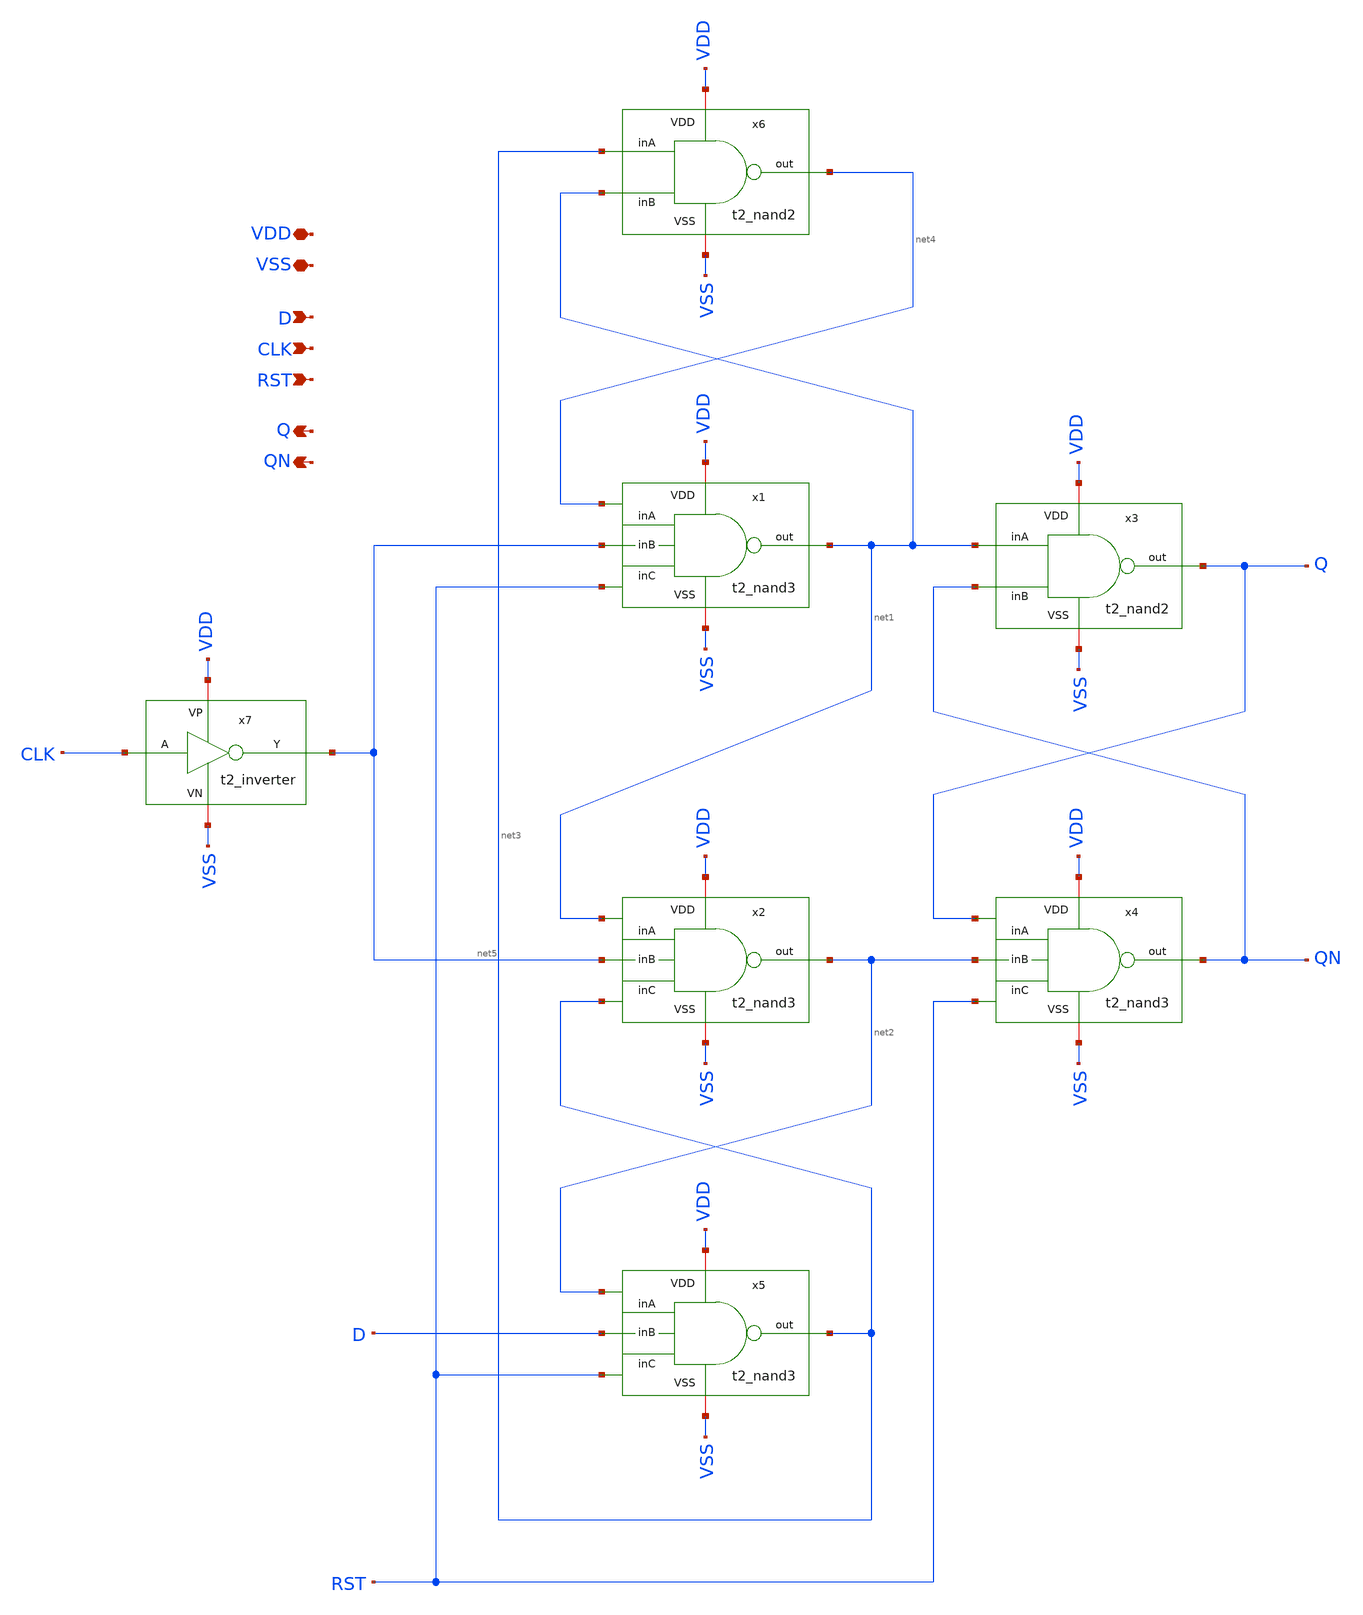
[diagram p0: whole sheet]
** sch_path: Team 2 Design/design_data/xschem/t2_dff_1.sch
**.subckt t2_dff_1 VSS D RST Q VDD QN CLK
*.iopin VSS
*.ipin D
*.ipin RST
*.opin Q
*.iopin VDD
*.opin QN
*.ipin CLK
x3 VDD net1 QN Q VSS t2_nand2
x4 VDD VSS Q net2 RST QN t2_nand3
x1 VDD VSS net4 net5 RST net1 t2_nand3
x2 VDD VSS net1 net5 net3 net2 t2_nand3
x6 VDD net3 net1 net4 VSS t2_nand2
x5 VDD VSS net2 D RST net3 t2_nand3
x7 VDD CLK net5 VSS t2_inverter
**.ends

* expanding   symbol:  t2_nand2.sym # of pins=5
** sym_path: Team 2 Design/design_data/xschem/t2_nand2.sym
** sch_path: Team 2 Design/design_data/xschem/t2_nand2.sch
.subckt t2_nand2 VDD inA inB out VSS
*.iopin VSS
*.ipin inA
*.ipin inB
*.opin out
*.iopin VDD
XM1 out inA VDD VDD sg13_lv_pmos w=0.3u l=0.13u ng=1 m=1 mm_ok=1
XM2 out inB VDD VDD sg13_lv_pmos w=0.3u l=0.13u ng=1 m=1 mm_ok=1
XM3 out inB net1 VSS sg13_lv_nmos w=0.15u l=0.13u ng=1 m=1 mm_ok=1
XM4 net1 inA VSS VSS sg13_lv_nmos w=0.15u l=0.13u ng=1 m=1 mm_ok=1
.ends


* expanding   symbol:  t2_nand3.sym # of pins=6
** sym_path: Team 2 Design/design_data/xschem/t2_nand3.sym
** sch_path: Team 2 Design/design_data/xschem/t2_nand3.sch
.subckt t2_nand3 VDD VSS inA inB inC out
*.iopin VSS
*.ipin inA
*.ipin inC
*.opin out
*.iopin VDD
*.ipin inB
XM1 out inB VDD VDD sg13_lv_pmos w=0.3u l=0.15u ng=1 m=1 mm_ok=1
XM2 out inC VDD VDD sg13_lv_pmos w=0.3u l=0.13u ng=1 m=1 mm_ok=1
XM3 out inC net1 VSS sg13_lv_nmos w=0.15u l=0.13u ng=1 m=1 mm_ok=1
XM4 net1 inB net2 VSS sg13_lv_nmos w=0.15u l=0.13u ng=1 m=1 mm_ok=1
XM5 net2 inA VSS VSS sg13_lv_nmos w=0.15u l=0.13u ng=1 m=1 mm_ok=1
XM0 out inA VDD VDD sg13_lv_pmos w=0.3u l=0.15u ng=1 m=1 mm_ok=1
.ends


* expanding   symbol:  t2_inverter.sym # of pins=4
** sym_path: Team 2 Design/design_data/xschem/t2_inverter.sym
** sch_path: Team 2 Design/design_data/xschem/t2_inverter.sch
.subckt t2_inverter VP A Y VN
*.iopin VP
*.iopin VN
*.ipin A
*.opin Y
XM2 Y A VP VP sg13_lv_pmos w=0.3u l=0.13u ng=1 m=1 mm_ok=1
XM1 Y A VN VN sg13_lv_nmos w=0.15u l=0.13u ng=1 m=1 mm_ok=1
.ends

.end
